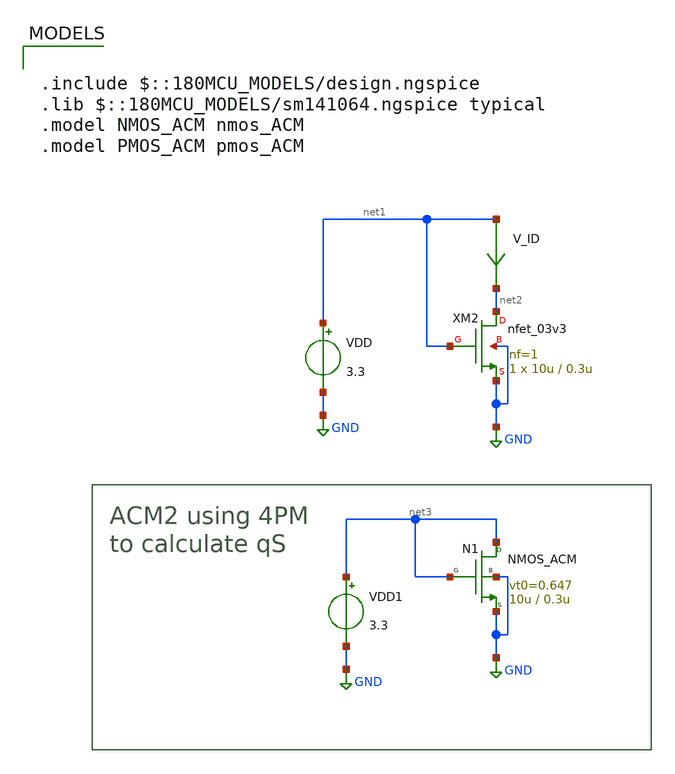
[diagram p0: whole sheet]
** sch_path: legacy/Examples/GF180MCU/xschem/Extraction/nmos_zeta.sch
**.subckt nmos_zeta
VDD net1 GND 3.3
V_ID net1 net2 0
.save i(v_id)
VDD1 net3 GND 3.3
XM2 net2 net1 GND GND nfet_03v3 L=0.3u W=10u nf=1 ad='int((nf+1)/2) * W/nf * 0.18u' as='int((nf+2)/2) * W/nf * 0.18u'
+ pd='2*int((nf+1)/2) * (W/nf + 0.18u)' ps='2*int((nf+2)/2) * (W/nf + 0.18u)' nrd='0.18u / W' nrs='0.18u / W'
+ sa=0 sb=0 sd=0 m=1
N1 net3 net3 GND GND NMOS_ACM w=10u l=0.3u n=1.37 is=2.15u vt0=0.647 sigma=26m zeta=1p
**** begin user architecture code

.include $::180MCU_MODELS/design.ngspice
.lib $::180MCU_MODELS/sm141064.ngspice typical
.model NMOS_ACM nmos_ACM
.model PMOS_ACM pmos_ACM




.control
pre_osdi ./NMOS_ACM_2V0.osdi
save all

op

let IDsat_=i(V_ID)
save IDsat_

let IS=@n1[is]
save IS

let qS=@n1[qS_op]
save qS

let idsat=IDsat_/IS
save idsat

let sqr=sqrt(1+idsat)
save sqr

let aux1 = 2*(qS+1-sqr)
save aux1

let zeta = aux1/idsat
save zeta

set appenwrite
write nmos_zeta.raw

.endc


**** end user architecture code
**.ends
.GLOBAL GND
.end
